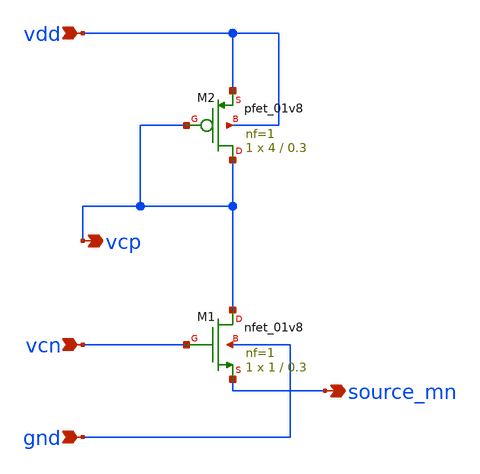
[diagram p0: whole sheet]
** sch_path: xsch/bias_ctrl.sch
**.subckt bias_ctrl vcn vdd gnd vcp source_mn
*.ipin vcn
*.ipin vdd
*.ipin gnd
*.opin vcp
*.opin source_mn
XM2 vcp vcp vdd vdd sky130_fd_pr__pfet_01v8 L=0.3 W=4 nf=1 ad='int((nf+1)/2) * W/nf * 0.29' as='int((nf+2)/2) * W/nf * 0.29'
+ pd='2*int((nf+1)/2) * (W/nf + 0.29)' ps='2*int((nf+2)/2) * (W/nf + 0.29)' nrd='0.29 / W' nrs='0.29 / W'
+ sa=0 sb=0 sd=0 mult=1 m=1
XM1 vcp vcn source_mn gnd sky130_fd_pr__nfet_01v8 L=0.3 W=1 nf=1 ad='int((nf+1)/2) * W/nf * 0.29' as='int((nf+2)/2) * W/nf * 0.29'
+ pd='2*int((nf+1)/2) * (W/nf + 0.29)' ps='2*int((nf+2)/2) * (W/nf + 0.29)' nrd='0.29 / W' nrs='0.29 / W'
+ sa=0 sb=0 sd=0 mult=1 m=1
**.ends
.end
